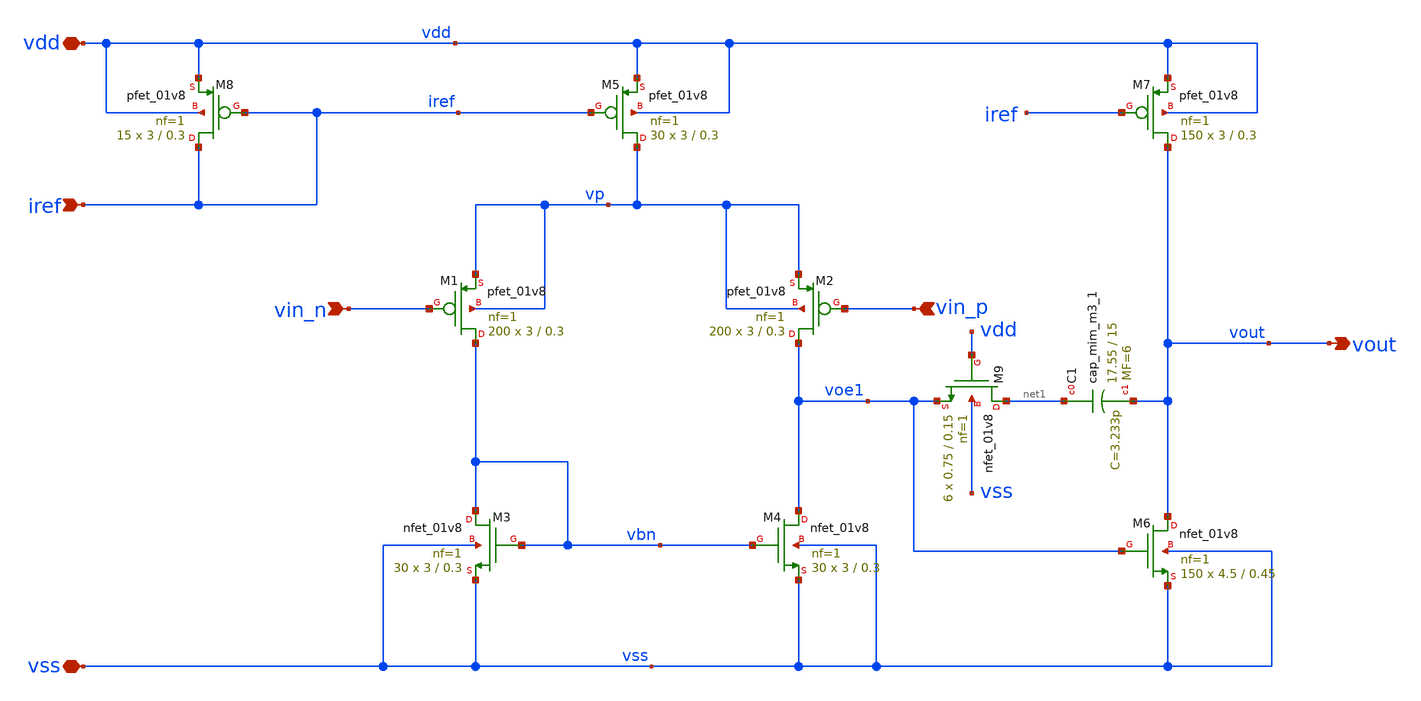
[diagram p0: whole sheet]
** sch_path: OPAMP/opamp_sky130.sch
**.subckt opamp_sky130 vdd vss vin_n vin_p iref vout
*.iopin vdd
*.iopin vss
*.ipin vin_n
*.ipin vin_p
*.ipin iref
*.opin vout
XM1 vbn vin_n vp vp sky130_fd_pr__pfet_01v8 L=0.3 W=3 nf=1 ad='W * 0.29' as='W * 0.29' pd='2 * (W + 0.29)'
+ ps='2 * (W + 0.29)' nrd='0.29 / W' nrs='0.29 / W' sa=0 sb=0 sd=0 mult=200 m=200
XM2 voe1 vin_p vp vp sky130_fd_pr__pfet_01v8 L=0.3 W=3 nf=1 ad='W * 0.29' as='W * 0.29' pd='2 * (W + 0.29)'
+ ps='2 * (W + 0.29)' nrd='0.29 / W' nrs='0.29 / W' sa=0 sb=0 sd=0 mult=200 m=200
XM3 vbn vbn vss vss sky130_fd_pr__nfet_01v8 L=0.3 W=3 nf=1 ad='W * 0.29' as='W * 0.29' pd='2 * (W + 0.29)'
+ ps='2 * (W + 0.29)' nrd='0.29 / W' nrs='0.29 / W' sa=0 sb=0 sd=0 mult=30 m=30
XM4 voe1 vbn vss vss sky130_fd_pr__nfet_01v8 L=0.3 W=3 nf=1 ad='W * 0.29' as='W * 0.29' pd='2 * (W + 0.29)'
+ ps='2 * (W + 0.29)' nrd='0.29 / W' nrs='0.29 / W' sa=0 sb=0 sd=0 mult=30 m=30
XM5 vp iref vdd vdd sky130_fd_pr__pfet_01v8 L=0.3 W=3 nf=1 ad='W * 0.29' as='W * 0.29' pd='2 * (W + 0.29)'
+ ps='2 * (W + 0.29)' nrd='0.29 / W' nrs='0.29 / W' sa=0 sb=0 sd=0 mult=30 m=30
XM7 vout iref vdd vdd sky130_fd_pr__pfet_01v8 L=0.3 W=3 nf=1 ad='W * 0.29' as='W * 0.29' pd='2 * (W + 0.29)'
+ ps='2 * (W + 0.29)' nrd='0.29 / W' nrs='0.29 / W' sa=0 sb=0 sd=0 mult=150 m=150
XM8 iref iref vdd vdd sky130_fd_pr__pfet_01v8 L=0.3 W=3 nf=1 ad='W * 0.29' as='W * 0.29' pd='2 * (W + 0.29)'
+ ps='2 * (W + 0.29)' nrd='0.29 / W' nrs='0.29 / W' sa=0 sb=0 sd=0 mult=15 m=15
XM9 net1 vdd voe1 vss sky130_fd_pr__nfet_01v8 L=0.15 W=0.75 nf=1 ad='W * 0.29' as='W * 0.29' pd='2 * (W + 0.29)'
+ ps='2 * (W + 0.29)' nrd='0.29 / W' nrs='0.29 / W' sa=0 sb=0 sd=0 mult=6 m=6
XC1 net1 vout sky130_fd_pr__cap_mim_m3_1 W=17.55 L=15 MF=6 m=6
XM6 vout voe1 vss vss sky130_fd_pr__nfet_01v8 L=0.45 W=4.5 nf=1 ad='W * 0.29' as='W * 0.29' pd='2 * (W + 0.29)'
+ ps='2 * (W + 0.29)' nrd='0.29 / W' nrs='0.29 / W' sa=0 sb=0 sd=0 mult=150 m=150
**.ends
.end
